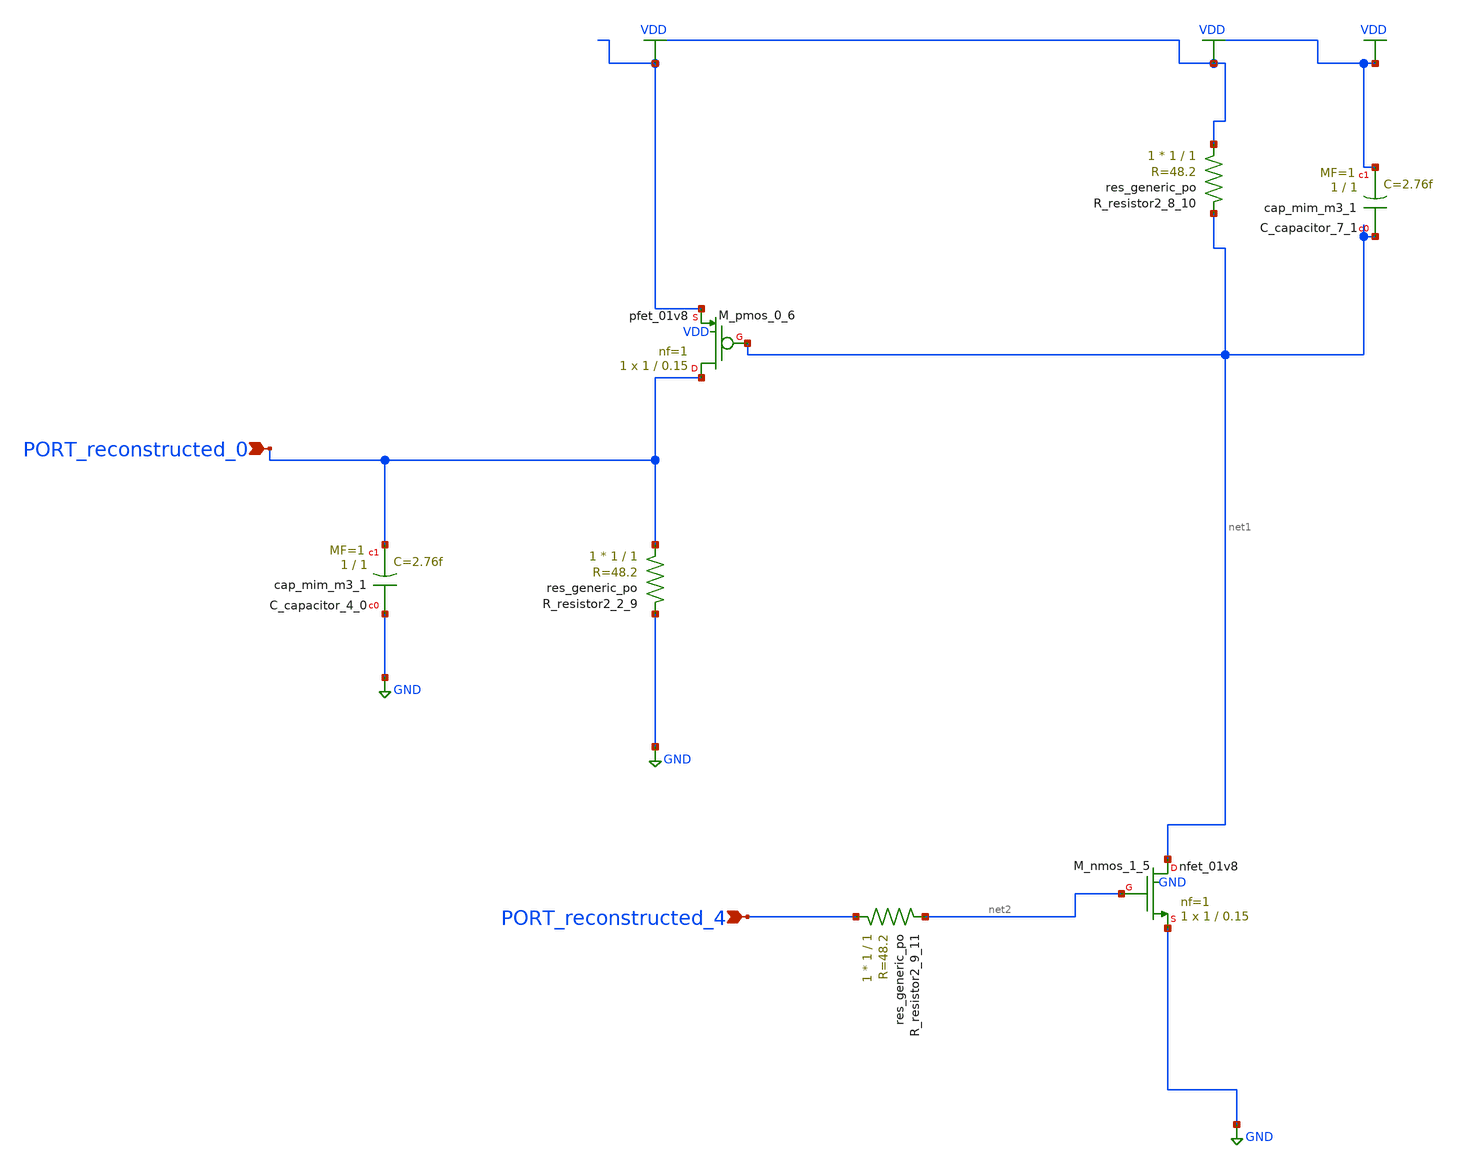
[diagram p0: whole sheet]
** sch_path: schematics/AMSNet/395.sch
**.subckt 395 PORT_reconstructed_4 PORT_reconstructed_0
*.ipin PORT_reconstructed_4
*.ipin PORT_reconstructed_0
XC_capacitor_4_0 GND PORT_reconstructed_0 sky130_fd_pr__cap_mim_m3_1 W=1 L=1 MF=1 m=1
XC_capacitor_7_1 net1 VDD sky130_fd_pr__cap_mim_m3_1 W=1 L=1 MF=1 m=1
XM_nmos_1_5 net1 net2 GND GND sky130_fd_pr__nfet_01v8 L=0.15 W=1 nf=1 ad='int((1 + 1)/2) * 1 / 1 * 0.29'
+ as='int((1 + 2)/2) * 1 / 1 * 0.29' pd='2*int((1 + 1)/2) * (1 / 1 + 0.29)' ps='2*int((1 + 2)/2) * (1 / 1 + 0.29)'
+ nrd='0.29 / 1 ' nrs='0.29 / 1 ' sa=0 sb=0 sd=0 mult=1 m=1
XM_pmos_0_6 PORT_reconstructed_0 net1 VDD VDD sky130_fd_pr__pfet_01v8 L=0.15 W=1 nf=1 ad='int((1 + 1)/2) * 1 / 1 * 0.29'
+ as='int((1 + 2)/2) * 1 / 1 * 0.29' pd='2*int((1 + 1)/2) * (1 / 1 + 0.29)' ps='2*int((1 + 2)/2) * (1 / 1 + 0.29)'
+ nrd='0.29 / 1 ' nrs='0.29 / 1 ' sa=0 sb=0 sd=0 mult=1 m=1
XR_resistor2_2_9 PORT_reconstructed_0 GND sky130_fd_pr__res_generic_po W=1 L=1 m=1
XR_resistor2_8_10 VDD net1 sky130_fd_pr__res_generic_po W=1 L=1 m=1
XR_resistor2_9_11 PORT_reconstructed_4 net2 sky130_fd_pr__res_generic_po W=1 L=1 m=1
**.ends
.GLOBAL GND
.GLOBAL VDD
.end
